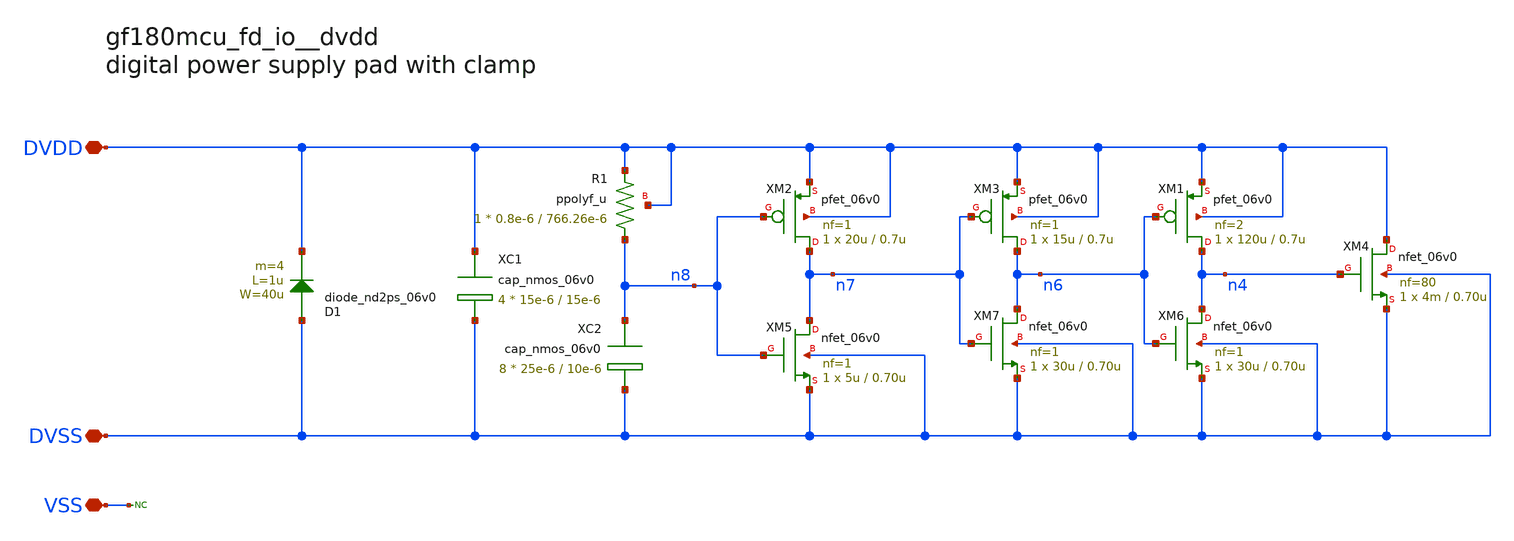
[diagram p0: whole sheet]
** sch_path: cells/dvdd/gf180mcu_fd_io__dvdd.sch
**.subckt gf180mcu_fd_io__dvdd DVDD DVSS VSS
*.iopin DVDD
*.iopin DVSS
*.iopin VSS
D1 DVSS DVDD diode_nd2ps_06v0 area='40u * 1u ' pj='2*40u + 2*1u ' m=4
XC1 DVDD DVSS cap_nmos_06v0 c_width=15e-6 c_length=15e-6 m=4
* noconn VSS
XM1 n4 n6 DVDD DVDD pfet_06v0 L=0.7u W=120u nf=2 ad='int((nf+1)/2) * W/nf * 0.18u' as='int((nf+2)/2) * W/nf * 0.18u'
+ pd='2*int((nf+1)/2) * (W/nf + 0.18u)' ps='2*int((nf+2)/2) * (W/nf + 0.18u)' nrd='0.18u / W' nrs='0.18u / W'
+ sa=0 sb=0 sd=0 m=1
XM2 n7 n8 DVDD DVDD pfet_06v0 L=0.7u W=20u nf=1 ad='int((nf+1)/2) * W/nf * 0.18u' as='int((nf+2)/2) * W/nf * 0.18u'
+ pd='2*int((nf+1)/2) * (W/nf + 0.18u)' ps='2*int((nf+2)/2) * (W/nf + 0.18u)' nrd='0.18u / W' nrs='0.18u / W'
+ sa=0 sb=0 sd=0 m=1
XM3 n6 n7 DVDD DVDD pfet_06v0 L=0.7u W=15u nf=1 ad='int((nf+1)/2) * W/nf * 0.18u' as='int((nf+2)/2) * W/nf * 0.18u'
+ pd='2*int((nf+1)/2) * (W/nf + 0.18u)' ps='2*int((nf+2)/2) * (W/nf + 0.18u)' nrd='0.18u / W' nrs='0.18u / W'
+ sa=0 sb=0 sd=0 m=1
XC2 n8 DVSS cap_nmos_06v0 c_width=25e-6 c_length=10e-6 m=8
XM4 DVDD n4 DVSS DVSS nfet_06v0 L=0.70u W=4m nf=80 ad='int((nf+1)/2) * W/nf * 0.18u' as='int((nf+2)/2) * W/nf * 0.18u'
+ pd='2*int((nf+1)/2) * (W/nf + 0.18u)' ps='2*int((nf+2)/2) * (W/nf + 0.18u)' nrd='0.18u / W' nrs='0.18u / W'
+ sa=0 sb=0 sd=0 m=1
XM5 n7 n8 DVSS DVSS nfet_06v0 L=0.70u W=5u nf=1 ad='int((nf+1)/2) * W/nf * 0.18u' as='int((nf+2)/2) * W/nf * 0.18u'
+ pd='2*int((nf+1)/2) * (W/nf + 0.18u)' ps='2*int((nf+2)/2) * (W/nf + 0.18u)' nrd='0.18u / W' nrs='0.18u / W'
+ sa=0 sb=0 sd=0 m=1
XM6 n4 n6 DVSS DVSS nfet_06v0 L=0.70u W=30u nf=1 ad='int((nf+1)/2) * W/nf * 0.18u' as='int((nf+2)/2) * W/nf * 0.18u'
+ pd='2*int((nf+1)/2) * (W/nf + 0.18u)' ps='2*int((nf+2)/2) * (W/nf + 0.18u)' nrd='0.18u / W' nrs='0.18u / W'
+ sa=0 sb=0 sd=0 m=1
XM7 n6 n7 DVSS DVSS nfet_06v0 L=0.70u W=30u nf=1 ad='int((nf+1)/2) * W/nf * 0.18u' as='int((nf+2)/2) * W/nf * 0.18u'
+ pd='2*int((nf+1)/2) * (W/nf + 0.18u)' ps='2*int((nf+2)/2) * (W/nf + 0.18u)' nrd='0.18u / W' nrs='0.18u / W'
+ sa=0 sb=0 sd=0 m=1
XR1 n8 DVDD DVDD ppolyf_u r_width=0.8e-6 r_length=766.26e-6 m=1
**.ends
.end
